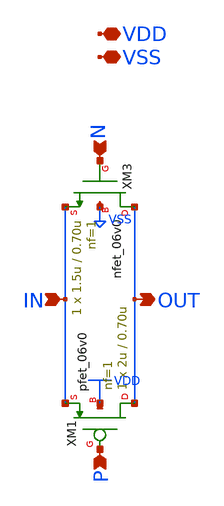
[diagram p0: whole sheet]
** sch_path: xschem/io_xfer_1i.sch
* Copyright 2023 David Mitchell Bailey
* Licensed under the Apache License, Version 2.0 (the "License");
* you may not use this file except in compliance with the License.
* You may obtain a copy of the License at
* https://www.apache.org/licenses/LICENSE-2.0
* Unless required by applicable law or agreed to in writing, software
* distributed under the License is distributed on an "AS IS" BASIS,
* WITHOUT WARRANTIES OR CONDITIONS OF ANY KIND, either express or implied.
* See the License for the specific language governing permissions and
* limitations under the License.
**.subckt io_xfer_1i OUT IN N P VDD VSS
*.opin OUT
*.ipin IN
*.ipin N
*.ipin P
*.iopin VDD
*.iopin VSS
XM1 OUT P IN VDD pfet_06v0 L=0.70u W=2u nf=1 ad='int((nf+1)/2) * W/nf * 0.18u' as='int((nf+2)/2) * W/nf * 0.18u'
+ pd='2*int((nf+1)/2) * (W/nf + 0.18u)' ps='2*int((nf+2)/2) * (W/nf + 0.18u)' nrd='0.18u / W' nrs='0.18u / W'
+ sa=0 sb=0 sd=0 m=1
XM3 OUT N IN VSS nfet_06v0 L=0.70u W=1.5u nf=1 ad='int((nf+1)/2) * W/nf * 0.18u' as='int((nf+2)/2) * W/nf * 0.18u'
+ pd='2*int((nf+1)/2) * (W/nf + 0.18u)' ps='2*int((nf+2)/2) * (W/nf + 0.18u)' nrd='0.18u / W' nrs='0.18u / W'
+ sa=0 sb=0 sd=0 m=1 par=1
**.ends
.GLOBAL VDD
.end
